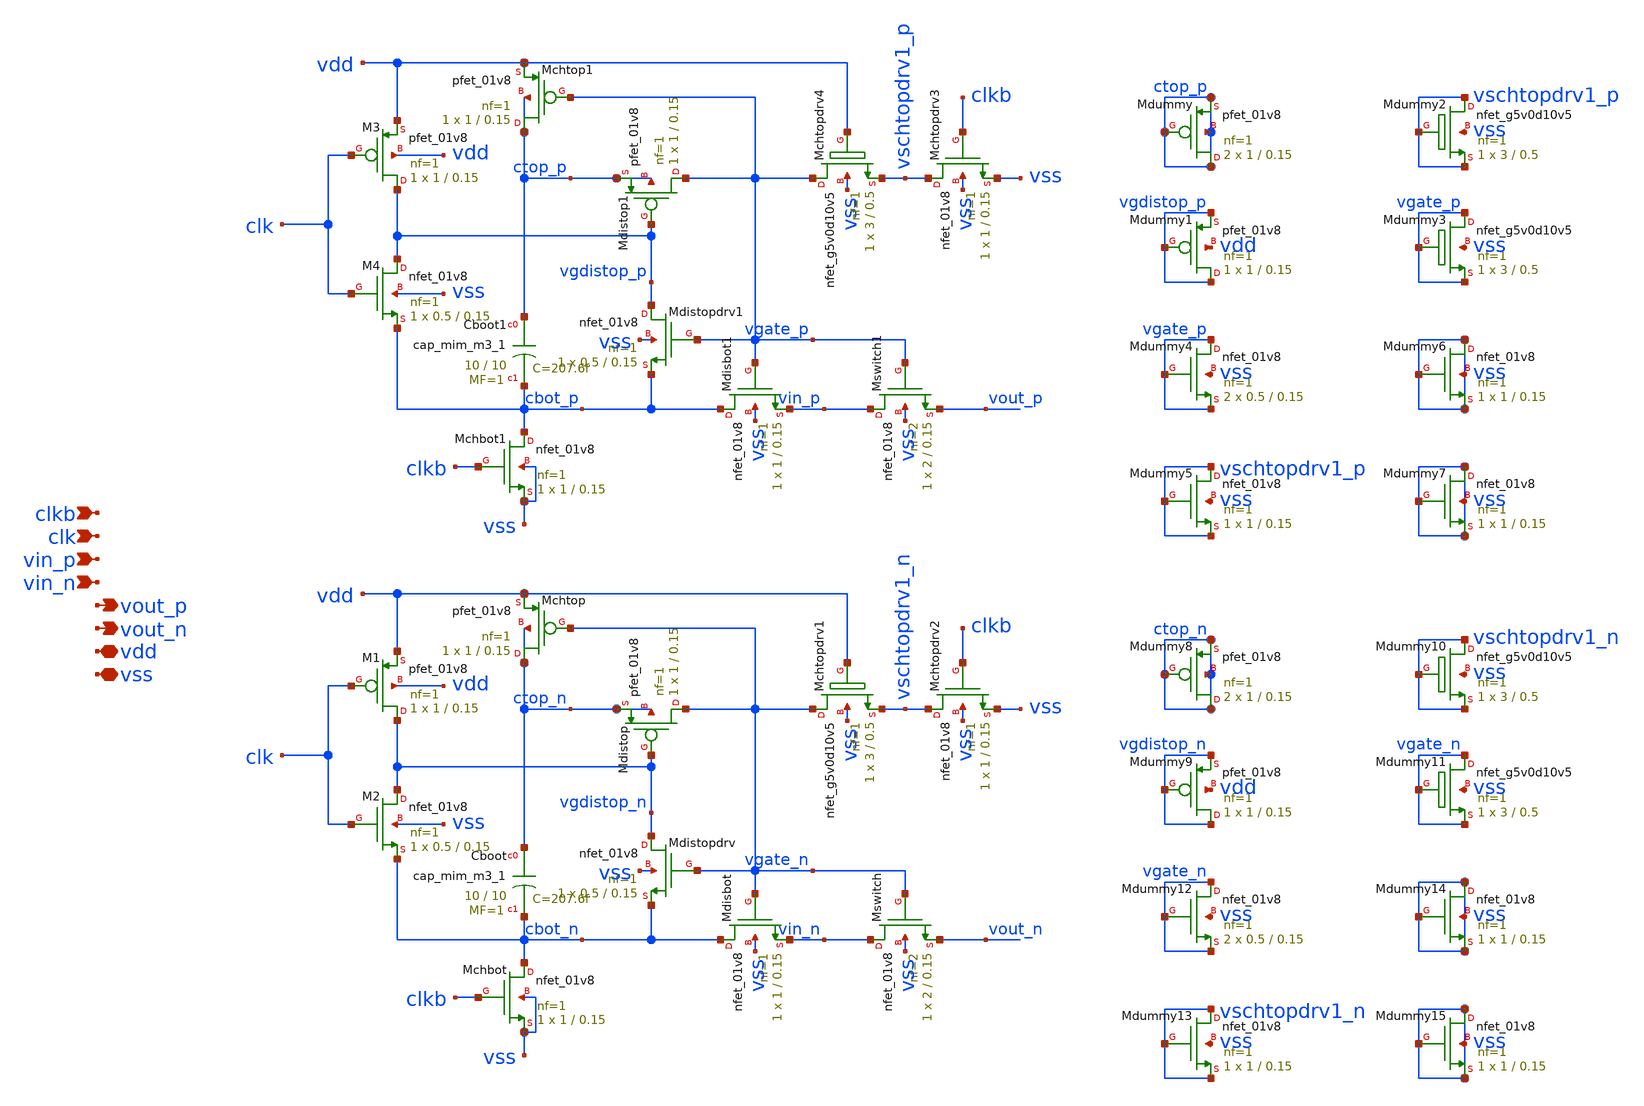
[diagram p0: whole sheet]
** sch_path: xschem/sar-adc/bootstrap.sch
**.subckt bootstrap clk vin_n vout_p vdd vss vin_p vout_n clkb
*.ipin clk
*.ipin vin_n
*.opin vout_p
*.iopin vdd
*.iopin vss
*.ipin vin_p
*.opin vout_n
*.ipin clkb
XMswitch vin_n vgate_n vout_n vss sky130_fd_pr__nfet_01v8 L=0.15 W=2 nf=2 ad='int((2 + 1)/2) * 2 / 2 * 0.29'
+ as='int((2 + 2)/2) * 2 / 2 * 0.29' pd='2*int((2 + 1)/2) * (2 / 2 + 0.29)' ps='2*int((2 + 2)/2) * (2 / 2 + 0.29)'
+ nrd='0.29 / 2 ' nrs='0.29 / 2 ' sa=0 sb=0 sd=0 mult=1 m=1
XMdisbot cbot_n vgate_n vin_n vss sky130_fd_pr__nfet_01v8 L=0.15 W=1 nf=1 ad='int((1 + 1)/2) * 1 / 1 * 0.29'
+ as='int((1 + 2)/2) * 1 / 1 * 0.29' pd='2*int((1 + 1)/2) * (1 / 1 + 0.29)' ps='2*int((1 + 2)/2) * (1 / 1 + 0.29)'
+ nrd='0.29 / 1 ' nrs='0.29 / 1 ' sa=0 sb=0 sd=0 mult=1 m=1
XCboot ctop_n cbot_n sky130_fd_pr__cap_mim_m3_1 W=10 L=10 MF=1 m=1
XMdistop vgate_n vgdistop_n ctop_n ctop_n sky130_fd_pr__pfet_01v8 L=0.15 W=1 nf=1 ad='int((1 + 1)/2) * 1 / 1 * 0.29'
+ as='int((1 + 2)/2) * 1 / 1 * 0.29' pd='2*int((1 + 1)/2) * (1 / 1 + 0.29)' ps='2*int((1 + 2)/2) * (1 / 1 + 0.29)'
+ nrd='0.29 / 1 ' nrs='0.29 / 1 ' sa=0 sb=0 sd=0 mult=1 m=1
XMchtop ctop_n vgate_n vdd ctop_n sky130_fd_pr__pfet_01v8 L=0.15 W=1 nf=1 ad='int((1 + 1)/2) * 1 / 1 * 0.29'
+ as='int((1 + 2)/2) * 1 / 1 * 0.29' pd='2*int((1 + 1)/2) * (1 / 1 + 0.29)' ps='2*int((1 + 2)/2) * (1 / 1 + 0.29)'
+ nrd='0.29 / 1 ' nrs='0.29 / 1 ' sa=0 sb=0 sd=0 mult=1 m=1
XMdistopdrv vgdistop_n vgate_n cbot_n vss sky130_fd_pr__nfet_01v8 L=0.15 W=0.5 nf=1 ad='int((1 + 1)/2) * 0.5 / 1 * 0.29'
+ as='int((1 + 2)/2) * 0.5 / 1 * 0.29' pd='2*int((1 + 1)/2) * (0.5 / 1 + 0.29)' ps='2*int((1 + 2)/2) * (0.5 / 1 + 0.29)'
+ nrd='0.29 / 0.5 ' nrs='0.29 / 0.5 ' sa=0 sb=0 sd=0 mult=1 m=1
XMchtopdrv2 vschtopdrv1_n clkb vss vss sky130_fd_pr__nfet_01v8 L=0.15 W=1 nf=1 ad='int((1 + 1)/2) * 1 / 1 * 0.29'
+ as='int((1 + 2)/2) * 1 / 1 * 0.29' pd='2*int((1 + 1)/2) * (1 / 1 + 0.29)' ps='2*int((1 + 2)/2) * (1 / 1 + 0.29)'
+ nrd='0.29 / 1 ' nrs='0.29 / 1 ' sa=0 sb=0 sd=0 mult=1 m=1
XMchbot cbot_n clkb vss vss sky130_fd_pr__nfet_01v8 L=0.15 W=1 nf=1 ad='int((1 + 1)/2) * 1 / 1 * 0.29'
+ as='int((1 + 2)/2) * 1 / 1 * 0.29' pd='2*int((1 + 1)/2) * (1 / 1 + 0.29)' ps='2*int((1 + 2)/2) * (1 / 1 + 0.29)'
+ nrd='0.29 / 1 ' nrs='0.29 / 1 ' sa=0 sb=0 sd=0 mult=1 m=1
XM1 vgdistop_n clk vdd vdd sky130_fd_pr__pfet_01v8 L=0.15 W=1 nf=1 ad='int((1 + 1)/2) * 1 / 1 * 0.29'
+ as='int((1 + 2)/2) * 1 / 1 * 0.29' pd='2*int((1 + 1)/2) * (1 / 1 + 0.29)' ps='2*int((1 + 2)/2) * (1 / 1 + 0.29)'
+ nrd='0.29 / 1 ' nrs='0.29 / 1 ' sa=0 sb=0 sd=0 mult=1 m=1
XM2 vgdistop_n clk cbot_n vss sky130_fd_pr__nfet_01v8 L=0.15 W=0.5 nf=1 ad='int((1 + 1)/2) * 0.5 / 1 * 0.29'
+ as='int((1 + 2)/2) * 0.5 / 1 * 0.29' pd='2*int((1 + 1)/2) * (0.5 / 1 + 0.29)' ps='2*int((1 + 2)/2) * (0.5 / 1 + 0.29)'
+ nrd='0.29 / 0.5 ' nrs='0.29 / 0.5 ' sa=0 sb=0 sd=0 mult=1 m=1
XMchtopdrv1 vgate_n vdd vschtopdrv1_n vss sky130_fd_pr__nfet_g5v0d10v5 L=0.5 W=3 nf=1 ad='int((1 + 1)/2) * 3 / 1 * 0.29'
+ as='int((1 + 2)/2) * 3 / 1 * 0.29' pd='2*int((1 + 1)/2) * (3 / 1 + 0.29)' ps='2*int((1 + 2)/2) * (3 / 1 + 0.29)'
+ nrd='0.29 / 3 ' nrs='0.29 / 3 ' sa=0 sb=0 sd=0 mult=1 m=1
XMswitch1 vin_p vgate_p vout_p vss sky130_fd_pr__nfet_01v8 L=0.15 W=2 nf=2 ad='int((2 + 1)/2) * 2 / 2 * 0.29'
+ as='int((2 + 2)/2) * 2 / 2 * 0.29' pd='2*int((2 + 1)/2) * (2 / 2 + 0.29)' ps='2*int((2 + 2)/2) * (2 / 2 + 0.29)'
+ nrd='0.29 / 2 ' nrs='0.29 / 2 ' sa=0 sb=0 sd=0 mult=1 m=1
XMdisbot1 cbot_p vgate_p vin_p vss sky130_fd_pr__nfet_01v8 L=0.15 W=1 nf=1 ad='int((1 + 1)/2) * 1 / 1 * 0.29'
+ as='int((1 + 2)/2) * 1 / 1 * 0.29' pd='2*int((1 + 1)/2) * (1 / 1 + 0.29)' ps='2*int((1 + 2)/2) * (1 / 1 + 0.29)'
+ nrd='0.29 / 1 ' nrs='0.29 / 1 ' sa=0 sb=0 sd=0 mult=1 m=1
XCboot1 ctop_p cbot_p sky130_fd_pr__cap_mim_m3_1 W=10 L=10 MF=1 m=1
XMdistop1 vgate_p vgdistop_p ctop_p ctop_p sky130_fd_pr__pfet_01v8 L=0.15 W=1 nf=1 ad='int((1 + 1)/2) * 1 / 1 * 0.29'
+ as='int((1 + 2)/2) * 1 / 1 * 0.29' pd='2*int((1 + 1)/2) * (1 / 1 + 0.29)' ps='2*int((1 + 2)/2) * (1 / 1 + 0.29)'
+ nrd='0.29 / 1 ' nrs='0.29 / 1 ' sa=0 sb=0 sd=0 mult=1 m=1
XMchtop1 ctop_p vgate_p vdd ctop_p sky130_fd_pr__pfet_01v8 L=0.15 W=1 nf=1 ad='int((1 + 1)/2) * 1 / 1 * 0.29'
+ as='int((1 + 2)/2) * 1 / 1 * 0.29' pd='2*int((1 + 1)/2) * (1 / 1 + 0.29)' ps='2*int((1 + 2)/2) * (1 / 1 + 0.29)'
+ nrd='0.29 / 1 ' nrs='0.29 / 1 ' sa=0 sb=0 sd=0 mult=1 m=1
XMdistopdrv1 vgdistop_p vgate_p cbot_p vss sky130_fd_pr__nfet_01v8 L=0.15 W=0.5 nf=1 ad='int((1 + 1)/2) * 0.5 / 1 * 0.29'
+ as='int((1 + 2)/2) * 0.5 / 1 * 0.29' pd='2*int((1 + 1)/2) * (0.5 / 1 + 0.29)' ps='2*int((1 + 2)/2) * (0.5 / 1 + 0.29)'
+ nrd='0.29 / 0.5 ' nrs='0.29 / 0.5 ' sa=0 sb=0 sd=0 mult=1 m=1
XMchtopdrv3 vschtopdrv1_p clkb vss vss sky130_fd_pr__nfet_01v8 L=0.15 W=1 nf=1 ad='int((1 + 1)/2) * 1 / 1 * 0.29'
+ as='int((1 + 2)/2) * 1 / 1 * 0.29' pd='2*int((1 + 1)/2) * (1 / 1 + 0.29)' ps='2*int((1 + 2)/2) * (1 / 1 + 0.29)'
+ nrd='0.29 / 1 ' nrs='0.29 / 1 ' sa=0 sb=0 sd=0 mult=1 m=1
XMchbot1 cbot_p clkb vss vss sky130_fd_pr__nfet_01v8 L=0.15 W=1 nf=1 ad='int((1 + 1)/2) * 1 / 1 * 0.29'
+ as='int((1 + 2)/2) * 1 / 1 * 0.29' pd='2*int((1 + 1)/2) * (1 / 1 + 0.29)' ps='2*int((1 + 2)/2) * (1 / 1 + 0.29)'
+ nrd='0.29 / 1 ' nrs='0.29 / 1 ' sa=0 sb=0 sd=0 mult=1 m=1
XM3 vgdistop_p clk vdd vdd sky130_fd_pr__pfet_01v8 L=0.15 W=1 nf=1 ad='int((1 + 1)/2) * 1 / 1 * 0.29'
+ as='int((1 + 2)/2) * 1 / 1 * 0.29' pd='2*int((1 + 1)/2) * (1 / 1 + 0.29)' ps='2*int((1 + 2)/2) * (1 / 1 + 0.29)'
+ nrd='0.29 / 1 ' nrs='0.29 / 1 ' sa=0 sb=0 sd=0 mult=1 m=1
XM4 vgdistop_p clk cbot_p vss sky130_fd_pr__nfet_01v8 L=0.15 W=0.5 nf=1 ad='int((1 + 1)/2) * 0.5 / 1 * 0.29'
+ as='int((1 + 2)/2) * 0.5 / 1 * 0.29' pd='2*int((1 + 1)/2) * (0.5 / 1 + 0.29)' ps='2*int((1 + 2)/2) * (0.5 / 1 + 0.29)'
+ nrd='0.29 / 0.5 ' nrs='0.29 / 0.5 ' sa=0 sb=0 sd=0 mult=1 m=1
XMchtopdrv4 vgate_p vdd vschtopdrv1_p vss sky130_fd_pr__nfet_g5v0d10v5 L=0.5 W=3 nf=1 ad='int((1 + 1)/2) * 3 / 1 * 0.29'
+ as='int((1 + 2)/2) * 3 / 1 * 0.29' pd='2*int((1 + 1)/2) * (3 / 1 + 0.29)' ps='2*int((1 + 2)/2) * (3 / 1 + 0.29)'
+ nrd='0.29 / 3 ' nrs='0.29 / 3 ' sa=0 sb=0 sd=0 mult=1 m=1
XMdummy ctop_p ctop_p ctop_p ctop_p sky130_fd_pr__pfet_01v8 L=0.15 W=1 nf=1 ad='int((1 + 1)/2) * 1 / 1 * 0.29'
+ as='int((1 + 2)/2) * 1 / 1 * 0.29' pd='2*int((1 + 1)/2) * (1 / 1 + 0.29)' ps='2*int((1 + 2)/2) * (1 / 1 + 0.29)'
+ nrd='0.29 / 1 ' nrs='0.29 / 1 ' sa=0 sb=0 sd=0 mult=2 m=2
XMdummy1 vgdistop_p vgdistop_p vgdistop_p vdd sky130_fd_pr__pfet_01v8 L=0.15 W=1 nf=1 ad='int((1 + 1)/2) * 1 / 1 * 0.29'
+ as='int((1 + 2)/2) * 1 / 1 * 0.29' pd='2*int((1 + 1)/2) * (1 / 1 + 0.29)' ps='2*int((1 + 2)/2) * (1 / 1 + 0.29)'
+ nrd='0.29 / 1 ' nrs='0.29 / 1 ' sa=0 sb=0 sd=0 mult=1 m=1
XMdummy2 vschtopdrv1_p vschtopdrv1_p vschtopdrv1_p vss sky130_fd_pr__nfet_g5v0d10v5 L=0.5 W=3 nf=1 ad='int((1 + 1)/2) * 3 / 1 * 0.29'
+ as='int((1 + 2)/2) * 3 / 1 * 0.29' pd='2*int((1 + 1)/2) * (3 / 1 + 0.29)' ps='2*int((1 + 2)/2) * (3 / 1 + 0.29)'
+ nrd='0.29 / 3 ' nrs='0.29 / 3 ' sa=0 sb=0 sd=0 mult=1 m=1
XMdummy3 vgate_p vgate_p vgate_p vss sky130_fd_pr__nfet_g5v0d10v5 L=0.5 W=3 nf=1 ad='int((1 + 1)/2) * 3 / 1 * 0.29'
+ as='int((1 + 2)/2) * 3 / 1 * 0.29' pd='2*int((1 + 1)/2) * (3 / 1 + 0.29)' ps='2*int((1 + 2)/2) * (3 / 1 + 0.29)'
+ nrd='0.29 / 3 ' nrs='0.29 / 3 ' sa=0 sb=0 sd=0 mult=1 m=1
XMdummy4 vgate_p vgate_p vgate_p vss sky130_fd_pr__nfet_01v8 L=0.15 W=0.5 nf=1 ad='int((1 + 1)/2) * 0.5 / 1 * 0.29'
+ as='int((1 + 2)/2) * 0.5 / 1 * 0.29' pd='2*int((1 + 1)/2) * (0.5 / 1 + 0.29)' ps='2*int((1 + 2)/2) * (0.5 / 1 + 0.29)'
+ nrd='0.29 / 0.5 ' nrs='0.29 / 0.5 ' sa=0 sb=0 sd=0 mult=2 m=2
XMdummy5 vschtopdrv1_p vschtopdrv1_p vschtopdrv1_p vss sky130_fd_pr__nfet_01v8 L=0.15 W=1 nf=1 ad='int((1 + 1)/2) * 1 / 1 * 0.29'
+ as='int((1 + 2)/2) * 1 / 1 * 0.29' pd='2*int((1 + 1)/2) * (1 / 1 + 0.29)' ps='2*int((1 + 2)/2) * (1 / 1 + 0.29)'
+ nrd='0.29 / 1 ' nrs='0.29 / 1 ' sa=0 sb=0 sd=0 mult=1 m=1
XMdummy6 vss vss vss vss sky130_fd_pr__nfet_01v8 L=0.15 W=1 nf=1 ad='int((1 + 1)/2) * 1 / 1 * 0.29' as='int((1 + 2)/2) * 1 / 1 * 0.29'
+ pd='2*int((1 + 1)/2) * (1 / 1 + 0.29)' ps='2*int((1 + 2)/2) * (1 / 1 + 0.29)' nrd='0.29 / 1 ' nrs='0.29 / 1 '
+ sa=0 sb=0 sd=0 mult=1 m=1
XMdummy7 vss vss vss vss sky130_fd_pr__nfet_01v8 L=0.15 W=1 nf=1 ad='int((1 + 1)/2) * 1 / 1 * 0.29' as='int((1 + 2)/2) * 1 / 1 * 0.29'
+ pd='2*int((1 + 1)/2) * (1 / 1 + 0.29)' ps='2*int((1 + 2)/2) * (1 / 1 + 0.29)' nrd='0.29 / 1 ' nrs='0.29 / 1 '
+ sa=0 sb=0 sd=0 mult=1 m=1
XMdummy8 ctop_n ctop_n ctop_n ctop_n sky130_fd_pr__pfet_01v8 L=0.15 W=1 nf=1 ad='int((1 + 1)/2) * 1 / 1 * 0.29'
+ as='int((1 + 2)/2) * 1 / 1 * 0.29' pd='2*int((1 + 1)/2) * (1 / 1 + 0.29)' ps='2*int((1 + 2)/2) * (1 / 1 + 0.29)'
+ nrd='0.29 / 1 ' nrs='0.29 / 1 ' sa=0 sb=0 sd=0 mult=2 m=2
XMdummy9 vgdistop_n vgdistop_n vgdistop_n vdd sky130_fd_pr__pfet_01v8 L=0.15 W=1 nf=1 ad='int((1 + 1)/2) * 1 / 1 * 0.29'
+ as='int((1 + 2)/2) * 1 / 1 * 0.29' pd='2*int((1 + 1)/2) * (1 / 1 + 0.29)' ps='2*int((1 + 2)/2) * (1 / 1 + 0.29)'
+ nrd='0.29 / 1 ' nrs='0.29 / 1 ' sa=0 sb=0 sd=0 mult=1 m=1
XMdummy10 vschtopdrv1_n vschtopdrv1_n vschtopdrv1_n vss sky130_fd_pr__nfet_g5v0d10v5 L=0.5 W=3 nf=1 ad='int((1 + 1)/2) * 3 / 1 * 0.29'
+ as='int((1 + 2)/2) * 3 / 1 * 0.29' pd='2*int((1 + 1)/2) * (3 / 1 + 0.29)' ps='2*int((1 + 2)/2) * (3 / 1 + 0.29)'
+ nrd='0.29 / 3 ' nrs='0.29 / 3 ' sa=0 sb=0 sd=0 mult=1 m=1
XMdummy11 vgate_n vgate_n vgate_n vss sky130_fd_pr__nfet_g5v0d10v5 L=0.5 W=3 nf=1 ad='int((1 + 1)/2) * 3 / 1 * 0.29'
+ as='int((1 + 2)/2) * 3 / 1 * 0.29' pd='2*int((1 + 1)/2) * (3 / 1 + 0.29)' ps='2*int((1 + 2)/2) * (3 / 1 + 0.29)'
+ nrd='0.29 / 3 ' nrs='0.29 / 3 ' sa=0 sb=0 sd=0 mult=1 m=1
XMdummy12 vgate_n vgate_n vgate_n vss sky130_fd_pr__nfet_01v8 L=0.15 W=0.5 nf=1 ad='int((1 + 1)/2) * 0.5 / 1 * 0.29'
+ as='int((1 + 2)/2) * 0.5 / 1 * 0.29' pd='2*int((1 + 1)/2) * (0.5 / 1 + 0.29)' ps='2*int((1 + 2)/2) * (0.5 / 1 + 0.29)'
+ nrd='0.29 / 0.5 ' nrs='0.29 / 0.5 ' sa=0 sb=0 sd=0 mult=2 m=2
XMdummy13 vschtopdrv1_n vschtopdrv1_n vschtopdrv1_n vss sky130_fd_pr__nfet_01v8 L=0.15 W=1 nf=1 ad='int((1 + 1)/2) * 1 / 1 * 0.29'
+ as='int((1 + 2)/2) * 1 / 1 * 0.29' pd='2*int((1 + 1)/2) * (1 / 1 + 0.29)' ps='2*int((1 + 2)/2) * (1 / 1 + 0.29)'
+ nrd='0.29 / 1 ' nrs='0.29 / 1 ' sa=0 sb=0 sd=0 mult=1 m=1
XMdummy14 vss vss vss vss sky130_fd_pr__nfet_01v8 L=0.15 W=1 nf=1 ad='int((1 + 1)/2) * 1 / 1 * 0.29'
+ as='int((1 + 2)/2) * 1 / 1 * 0.29' pd='2*int((1 + 1)/2) * (1 / 1 + 0.29)' ps='2*int((1 + 2)/2) * (1 / 1 + 0.29)'
+ nrd='0.29 / 1 ' nrs='0.29 / 1 ' sa=0 sb=0 sd=0 mult=1 m=1
XMdummy15 vss vss vss vss sky130_fd_pr__nfet_01v8 L=0.15 W=1 nf=1 ad='int((1 + 1)/2) * 1 / 1 * 0.29'
+ as='int((1 + 2)/2) * 1 / 1 * 0.29' pd='2*int((1 + 1)/2) * (1 / 1 + 0.29)' ps='2*int((1 + 2)/2) * (1 / 1 + 0.29)'
+ nrd='0.29 / 1 ' nrs='0.29 / 1 ' sa=0 sb=0 sd=0 mult=1 m=1
**.ends
.end
